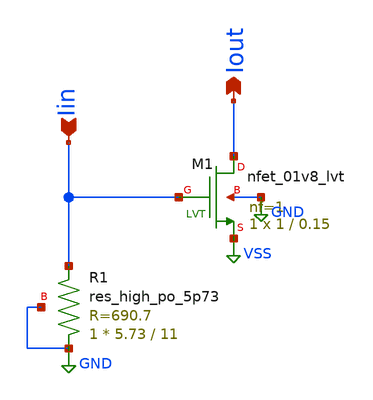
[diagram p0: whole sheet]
** sch_path: analog/schematics/components/LowAreaCell/LowArea_Cell.sch
**.subckt LowArea_Cell Iin Iout
*.ipin Iin
*.opin Iout
XM1 Iout Iin VSS GND sky130_fd_pr__nfet_01v8_lvt L=0.15 W=1 nf=1 ad='int((nf+1)/2) * W/nf * 0.29' as='int((nf+2)/2) * W/nf * 0.29'
+ pd='2*int((nf+1)/2) * (W/nf + 0.29)' ps='2*int((nf+2)/2) * (W/nf + 0.29)' nrd='0.29 / W' nrs='0.29 / W'
+ sa=0 sb=0 sd=0 mult=1 m=1
XR1 GND Iin GND sky130_fd_pr__res_high_po_5p73 L=11 mult=1 m=1
**.ends
.GLOBAL GND
.GLOBAL VSS
.end
